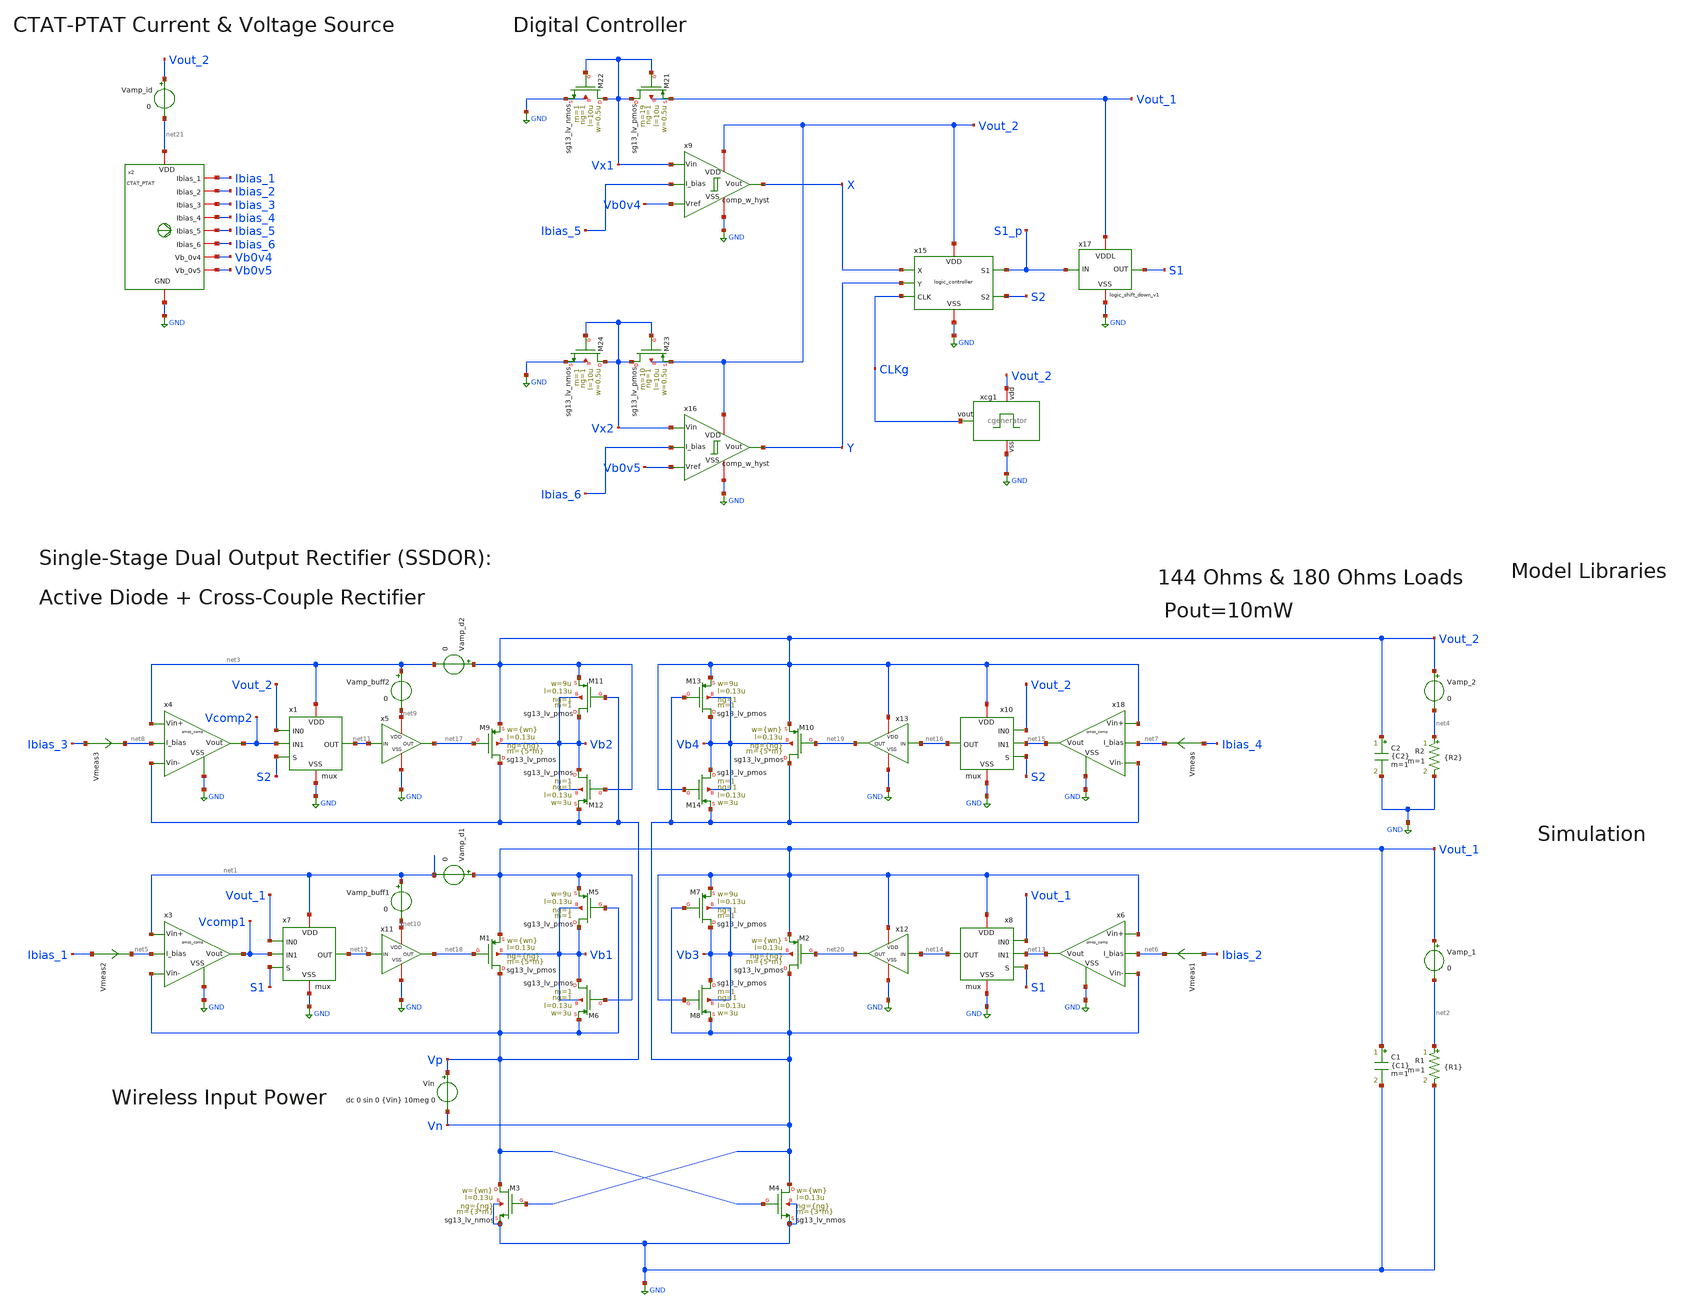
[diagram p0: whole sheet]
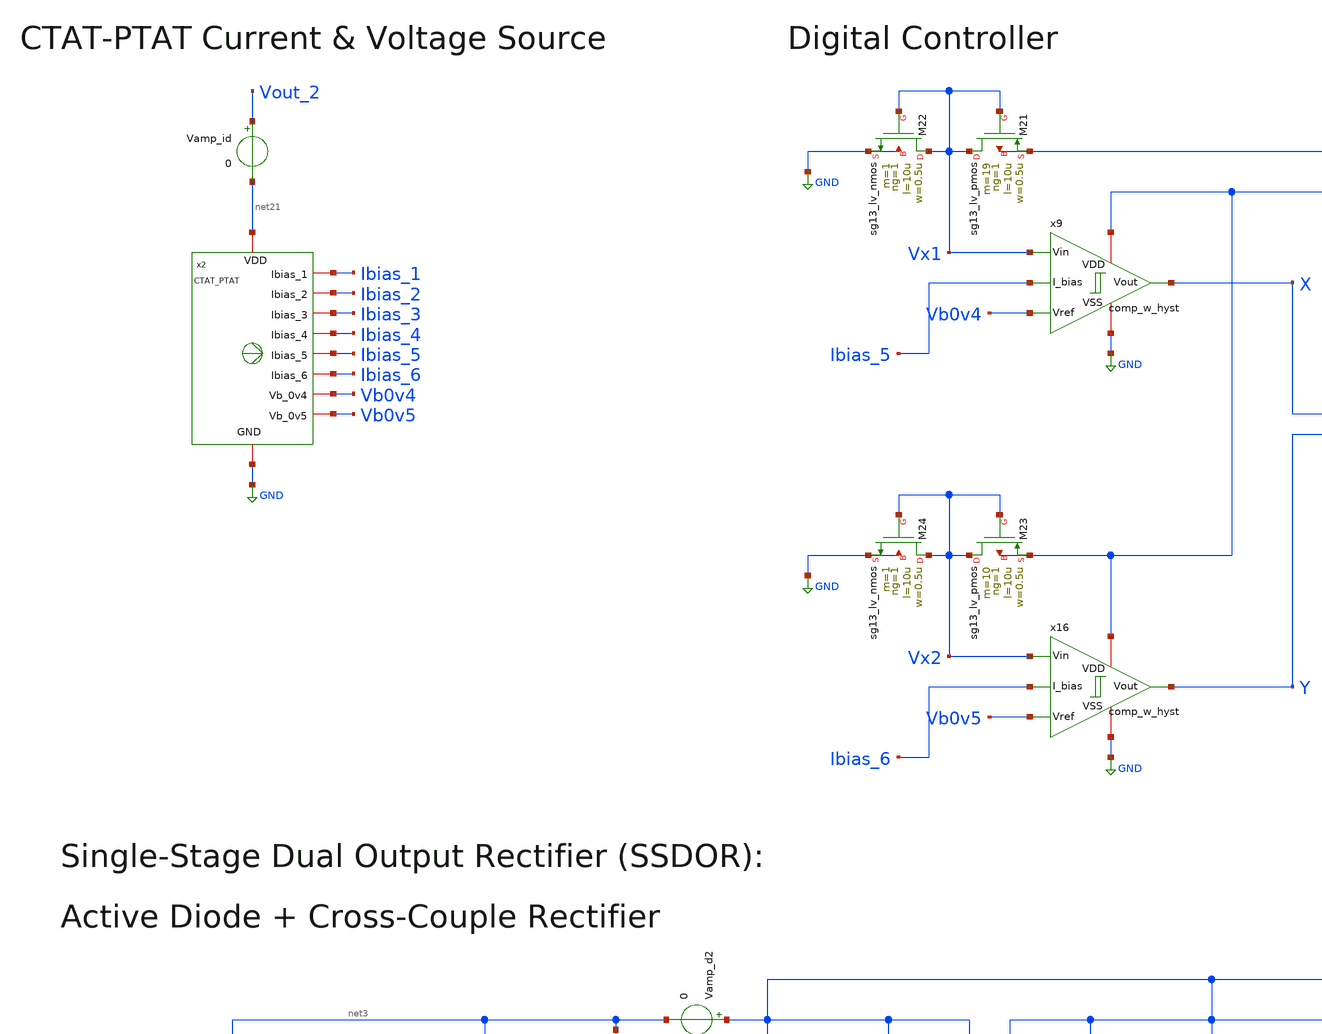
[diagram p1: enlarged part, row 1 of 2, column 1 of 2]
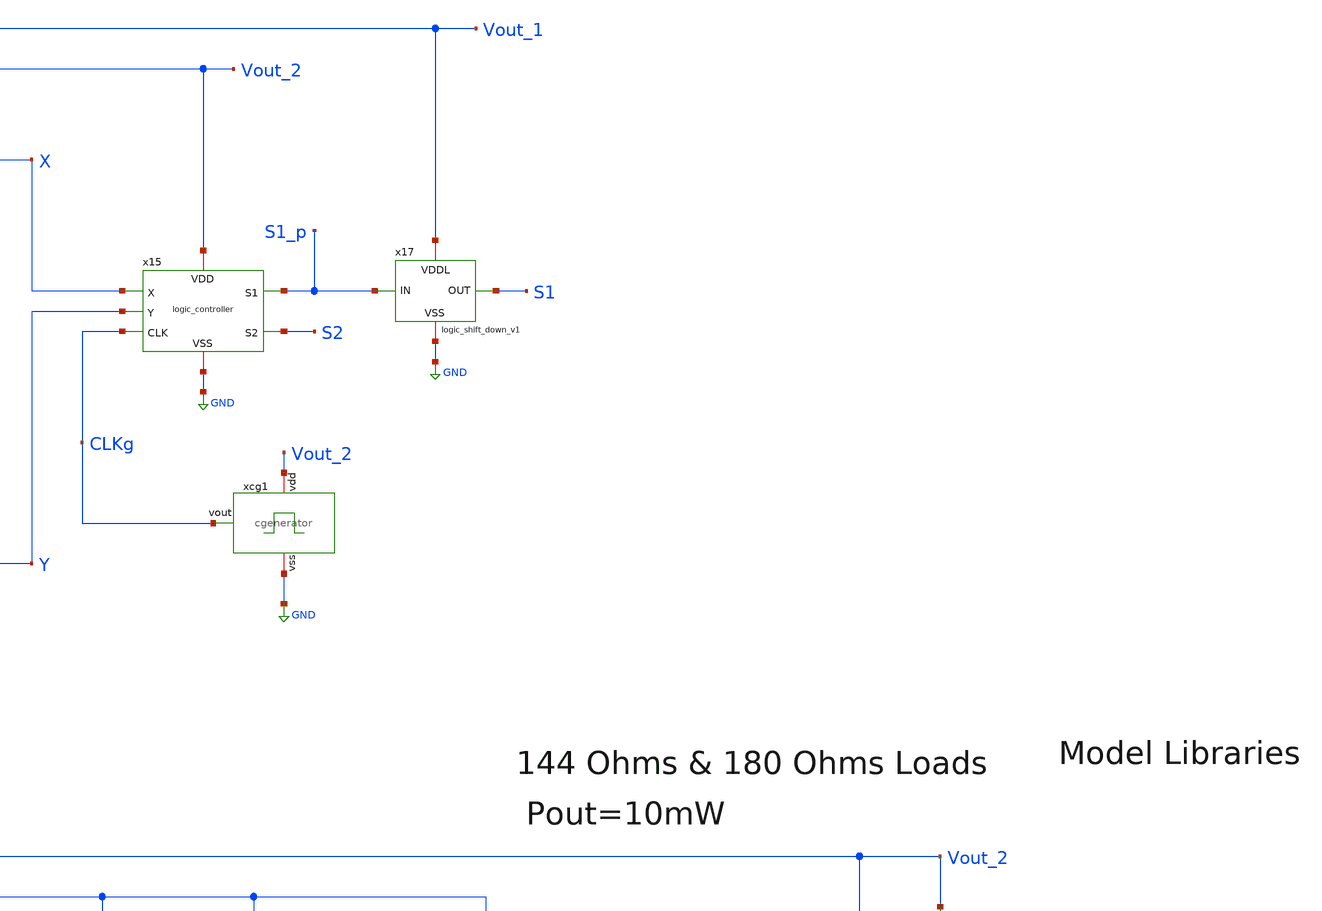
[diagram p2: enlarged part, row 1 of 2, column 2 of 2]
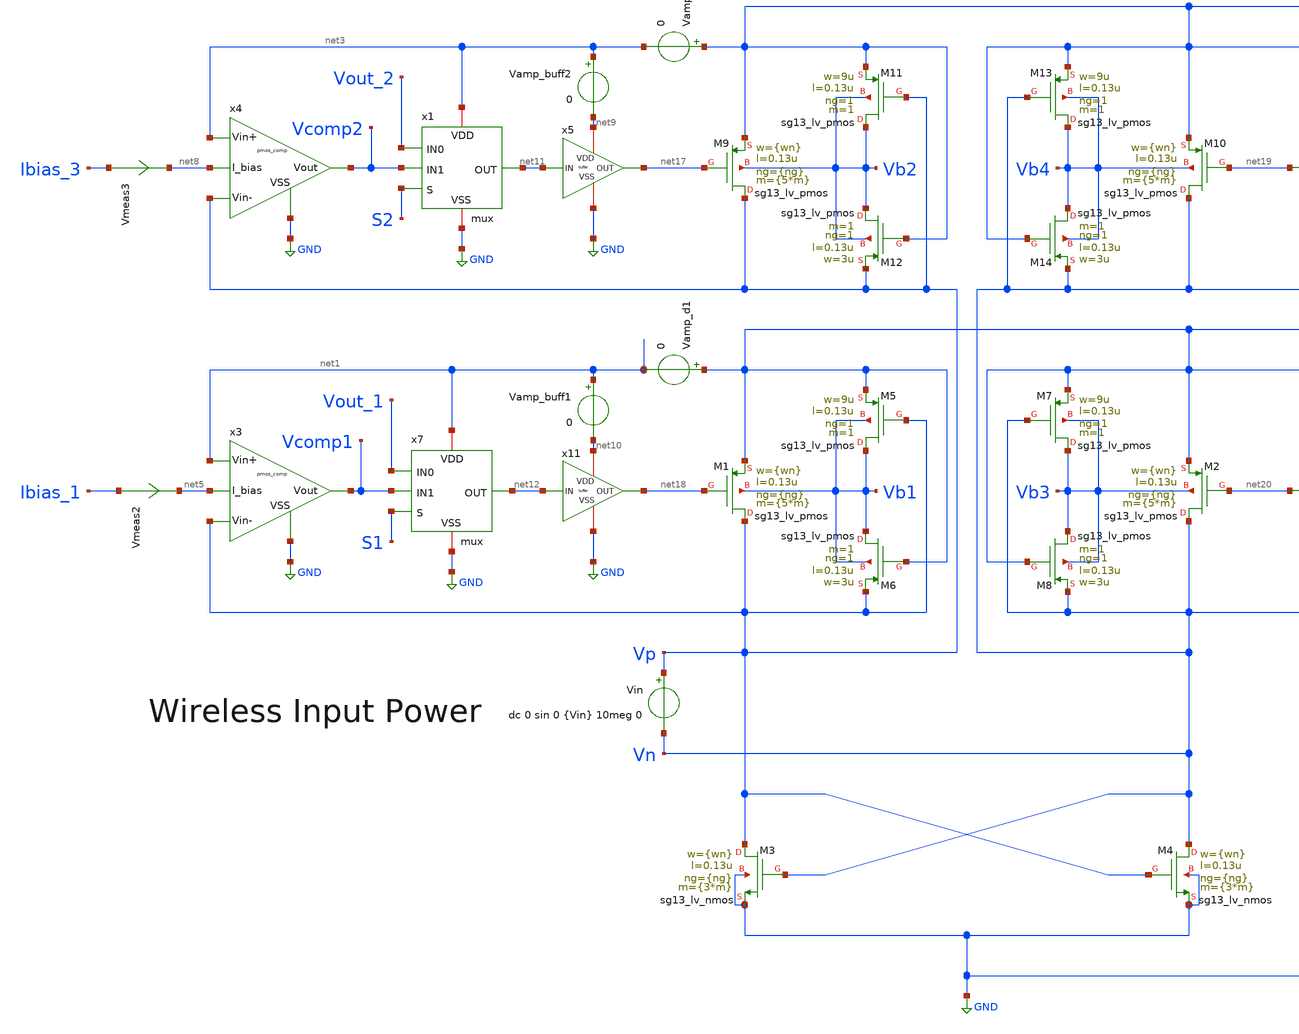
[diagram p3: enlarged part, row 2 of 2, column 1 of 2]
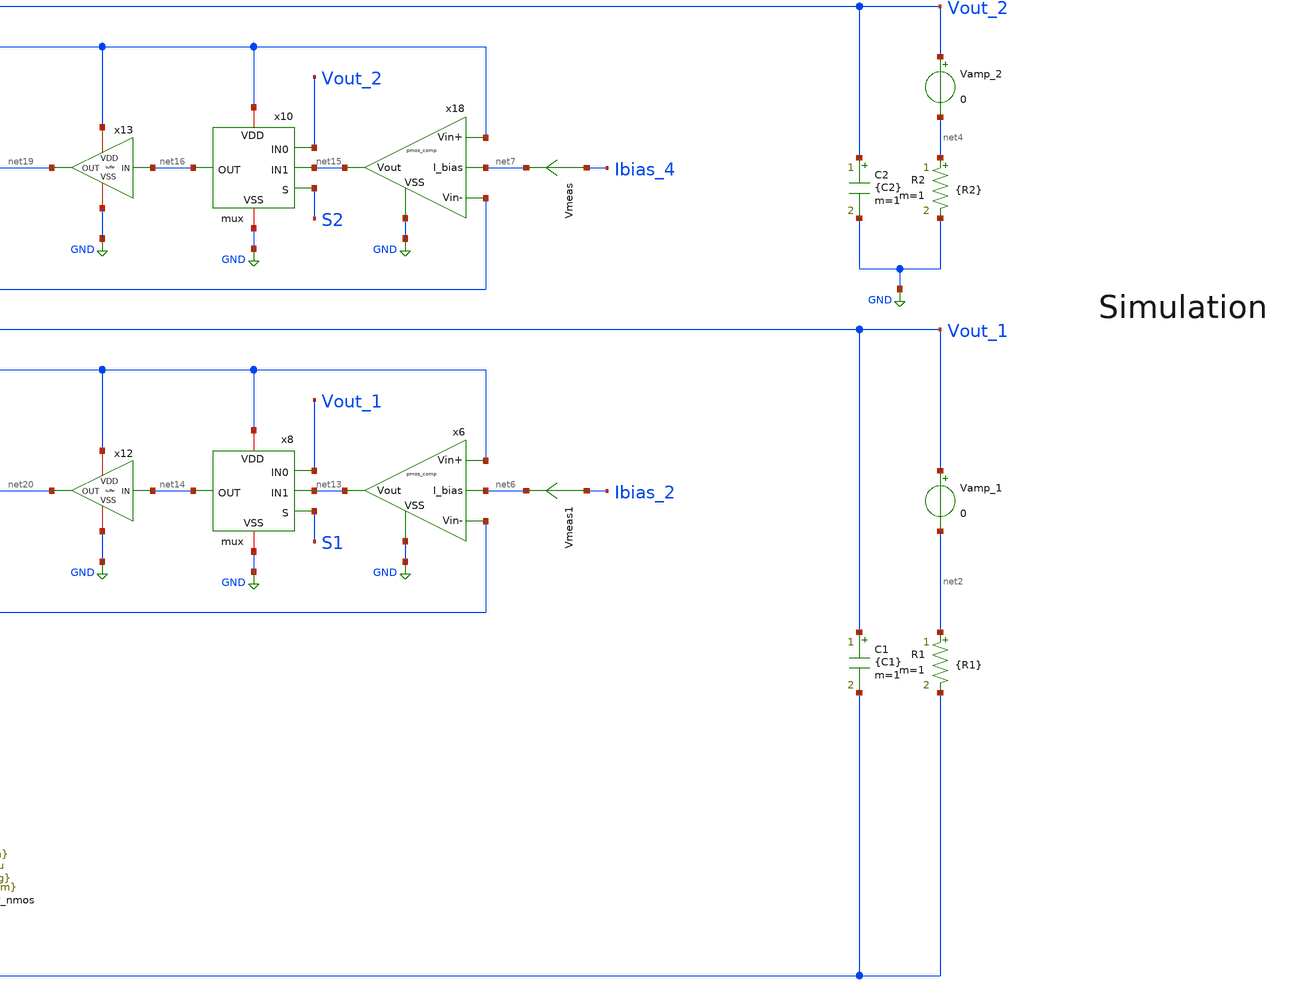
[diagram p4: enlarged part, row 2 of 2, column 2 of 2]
** sch_path: SSDOR_1.2V_v3/SSDOR_1.2V_v3_tb_pce_sweep.sch
**.subckt SSDOR_1.2V_v3_tb_pce_sweep
XM1 Vp net18 Vout_1 Vb1 sg13_lv_pmos w={wn} l=0.13u ng={ng} m={5*m} mm_ok=1
XM2 Vn net20 Vout_1 Vb3 sg13_lv_pmos w={wn} l=0.13u ng={ng} m={5*m} mm_ok=1
XM3 Vp Vn GND GND sg13_lv_nmos w={wn} l=0.13u ng={ng} m={3*m} mm_ok=1
XM4 Vn Vp GND GND sg13_lv_nmos w={wn} l=0.13u ng={ng} m={3*m} mm_ok=1
XM5 Vb1 Vp Vout_1 Vb1 sg13_lv_pmos w=9u l=0.13u ng=1 m=1 mm_ok=1
XM6 Vb1 Vout_1 Vp Vb1 sg13_lv_pmos w=3u l=0.13u ng=1 m=1 mm_ok=1
XM7 Vb3 Vn Vout_1 Vb3 sg13_lv_pmos w=9u l=0.13u ng=1 m=1 mm_ok=1
XM8 Vb3 Vout_1 Vn Vb3 sg13_lv_pmos w=3u l=0.13u ng=1 m=1 mm_ok=1
Vin Vp Vn dc 0 sin 0 {Vin} 10meg 0
C1 Vout_1 GND {C1} m=1
R1 net2 GND {R1} m=1
Vamp_1 Vout_1 net2 0
XM9 Vp net17 Vout_2 Vb2 sg13_lv_pmos w={wn} l=0.13u ng={ng} m={5*m} mm_ok=1
XM10 Vn net19 Vout_2 Vb4 sg13_lv_pmos w={wn} l=0.13u ng={ng} m={5*m} mm_ok=1
XM11 Vb2 Vp Vout_2 Vb2 sg13_lv_pmos w=9u l=0.13u ng=1 m=1 mm_ok=1
XM12 Vb2 Vout_2 Vp Vb2 sg13_lv_pmos w=3u l=0.13u ng=1 m=1 mm_ok=1
XM13 Vb4 Vn Vout_2 Vb4 sg13_lv_pmos w=9u l=0.13u ng=1 m=1 mm_ok=1
XM14 Vb4 Vout_2 Vn Vb4 sg13_lv_pmos w=3u l=0.13u ng=1 m=1 mm_ok=1
C2 Vout_2 GND {C2} m=1
R2 net4 GND {R2} m=1
Vamp_2 Vout_2 net4 0
XM21 Vx1 Vx1 Vout_1 Vout_1 sg13_lv_pmos w=0.5u l=10u ng=1 m=19 mm_ok=1
XM22 Vx1 Vx1 GND GND sg13_lv_nmos w=0.5u l=10u ng=1 m=1 mm_ok=1
XM23 Vx2 Vx2 Vout_2 Vout_2 sg13_lv_pmos w=0.5u l=10u ng=1 m=10 mm_ok=1
XM24 Vx2 Vx2 GND GND sg13_lv_nmos w=0.5u l=10u ng=1 m=1 mm_ok=1
Vamp_d2 Vout_2 net3 0
Vamp_d1 Vout_1 net1 0
Vamp_buff2 net3 net9 0
Vamp_buff1 net1 net10 0
Vmeas Ibias_4 net7 0
.save i(vmeas)
Vmeas1 Ibias_2 net6 0
.save i(vmeas1)
Vmeas2 Ibias_1 net5 0
.save i(vmeas2)
Vmeas3 Ibias_3 net8 0
.save i(vmeas3)
Vamp_id Vout_2 net21 0
x2 net21 GND Ibias_4 Ibias_1 Ibias_2 Ibias_5 Ibias_6 Ibias_3 Vb0v5 Vb0v4 CTAT_PTAT
x9 Vout_2 GND Vb0v4 Vx1 X Ibias_5 comp_w_hyst
x16 Vout_2 GND Vb0v5 Vx2 Y Ibias_6 comp_w_hyst
x15 Vout_2 X S1_p CLKg Y S2 GND logic_controller
x17 Vout_1 S1_p S1 GND logic_shift_down_v1
x3 Vp net1 Vcomp1 net5 GND pmos_comp
x4 Vp net3 Vcomp2 net8 GND pmos_comp
x18 Vn Vout_2 net15 net7 GND pmos_comp
x6 Vn Vout_1 net13 net6 GND pmos_comp
x1 net3 Vout_2 S2 net11 Vcomp2 GND mux
x7 net1 Vout_1 S1 net12 Vcomp1 GND mux
x8 Vout_1 Vout_1 S1 net14 net13 GND mux
x10 Vout_2 Vout_2 S2 net16 net15 GND mux
x5 net9 net11 net17 GND buffer wn=1u
x11 net10 net12 net18 GND buffer wn=1u
x12 Vout_1 net14 net20 GND buffer wn=1u
x13 Vout_2 net16 net19 GND buffer wn=1u
xcg1 Vout_2 CLKg GND cgenerator
**.ends
.GLOBAL GND
**** begin user architecture code



.lib cornerMOSlv.lib mos_tt
.lib cornerMOShv.lib mos_tt
.lib cornerRES.lib res_typ
.lib cornerCAP.lib cap_typ

.param R1=144
.param R2=180
.param C1=80n
.param C2=60n
.param Vin=1.2
.param wn=5u
.param ng=35
.param m=40

.control
 set color0 = white
 set t1 = 10u
 set t2 = 20u

 let r = 1000
 let i = 0
 let points = 1

 let pce_vec = vector(points)
 let r_vec = vector(points)
 let vcr1_vec = vector(points)
 let vcr2_vec = vector(points)
 let pout_vec = vector(points)


 while i < points

  alterparam R1 = r
  alterparam R2 = 1.25*r


  tran 80000p 20u

  meas tran v_reg_1 AVG v(vout_1) from=10u to=20u
  meas tran v_reg_2 AVG v(vout_2) from=10u to=20u
  meas tran p_out_1 AVG ((v(Vout_1)*v(Vout_1))/R1) from=10u to=20u
  meas tran p_out_2 AVG ((v(Vout_2)*v(Vout_2))/R2) from=10u to=20u
  meas tran p_out AVG (pout1 + pout2) from=10u to=20u
  meas tran p_in AVG (-(v(Vp)-v(Vn))*i(Vin)) from=10u to=20u


  let pce = p_out/p_in
  let vcr1 = v_reg_1/Vin
  let vcr2 = v_reg_2/Vin

  let r_vec[i] = r
  let pce_vec[i] = pce
  let vcr1_vec[i] = vcr1
  let vcr2_vec[i] = vcr2
  let pout_vec[i] = p_out

  let pce_vec[i] = pce
  let r_vec[i] = r

  let r = r + 1000
  let i = i + 1

 end

 setscale r_vec
 set xlog

 plot pce_vec title PCE

**** end user architecture code
.end
